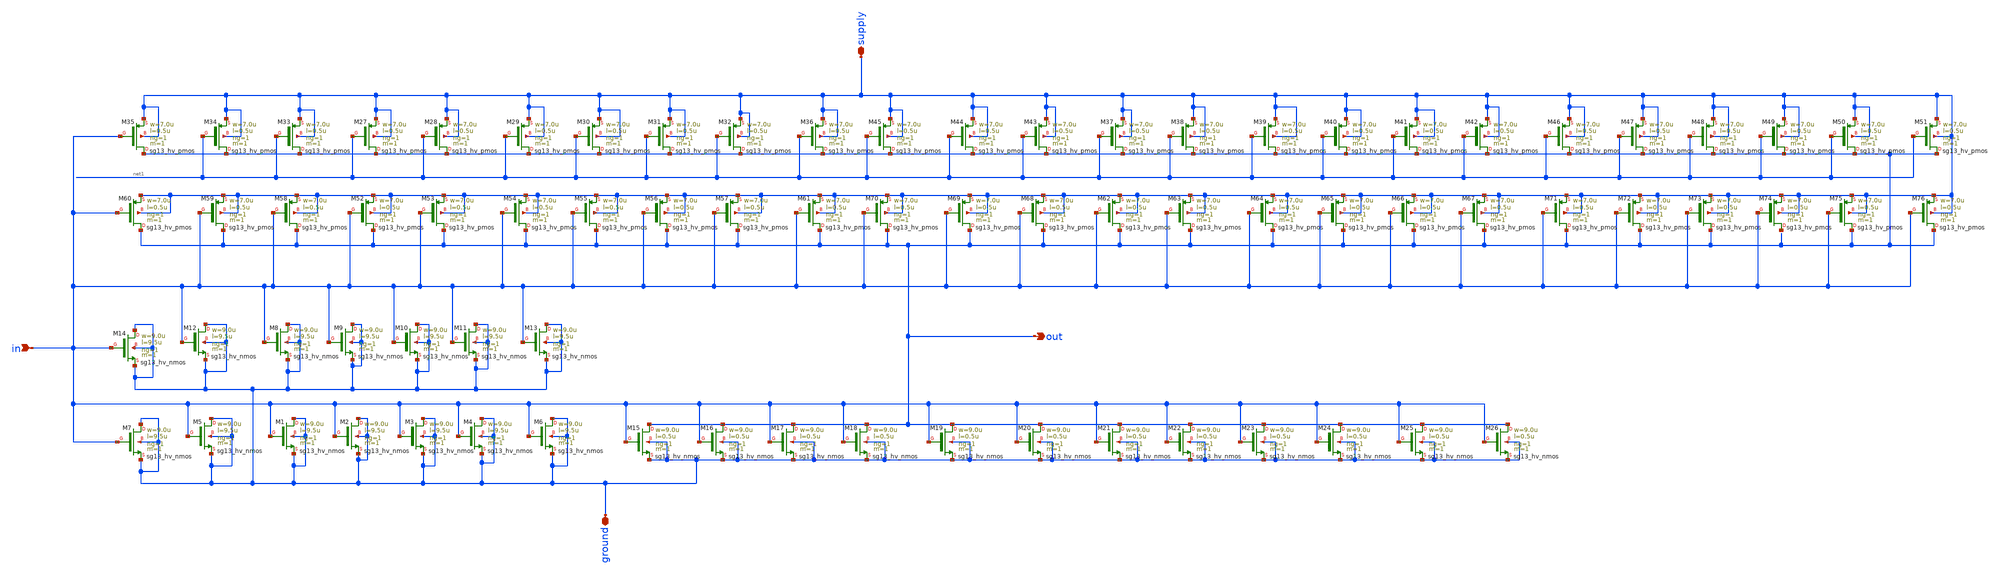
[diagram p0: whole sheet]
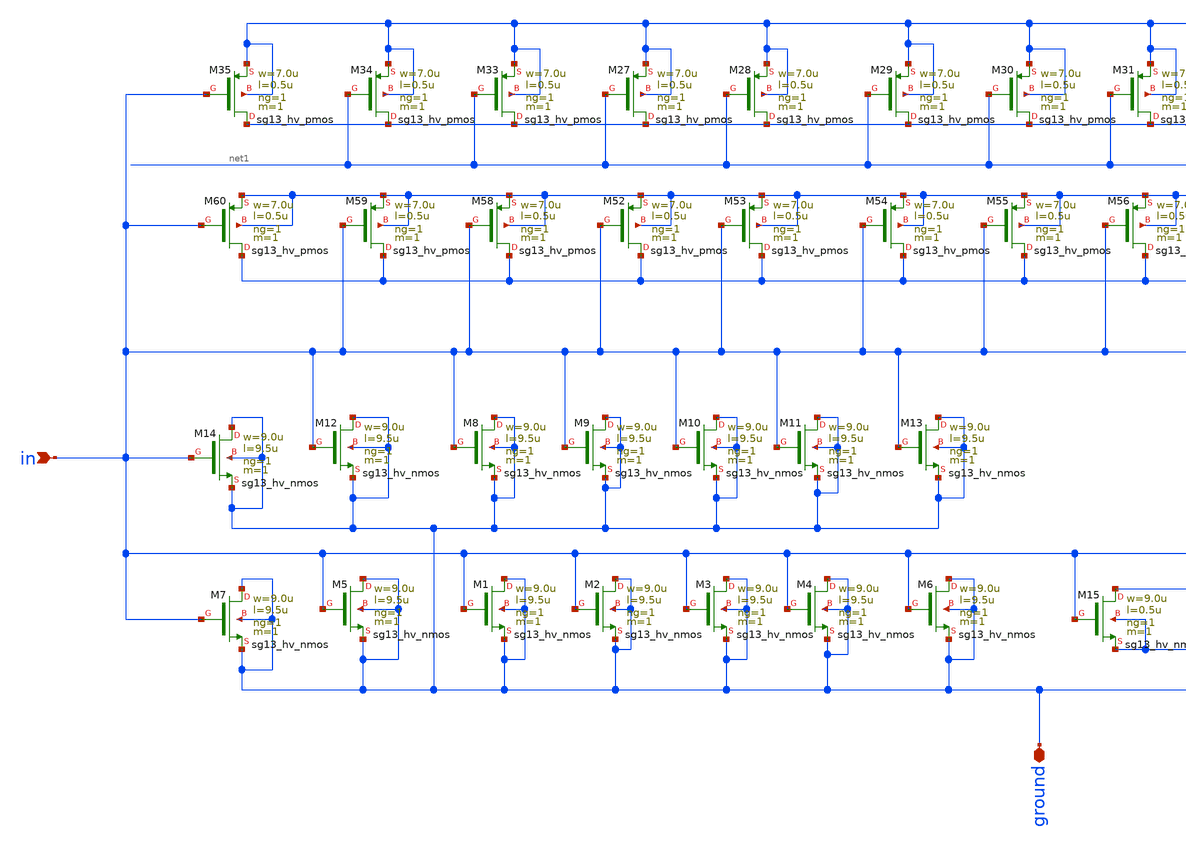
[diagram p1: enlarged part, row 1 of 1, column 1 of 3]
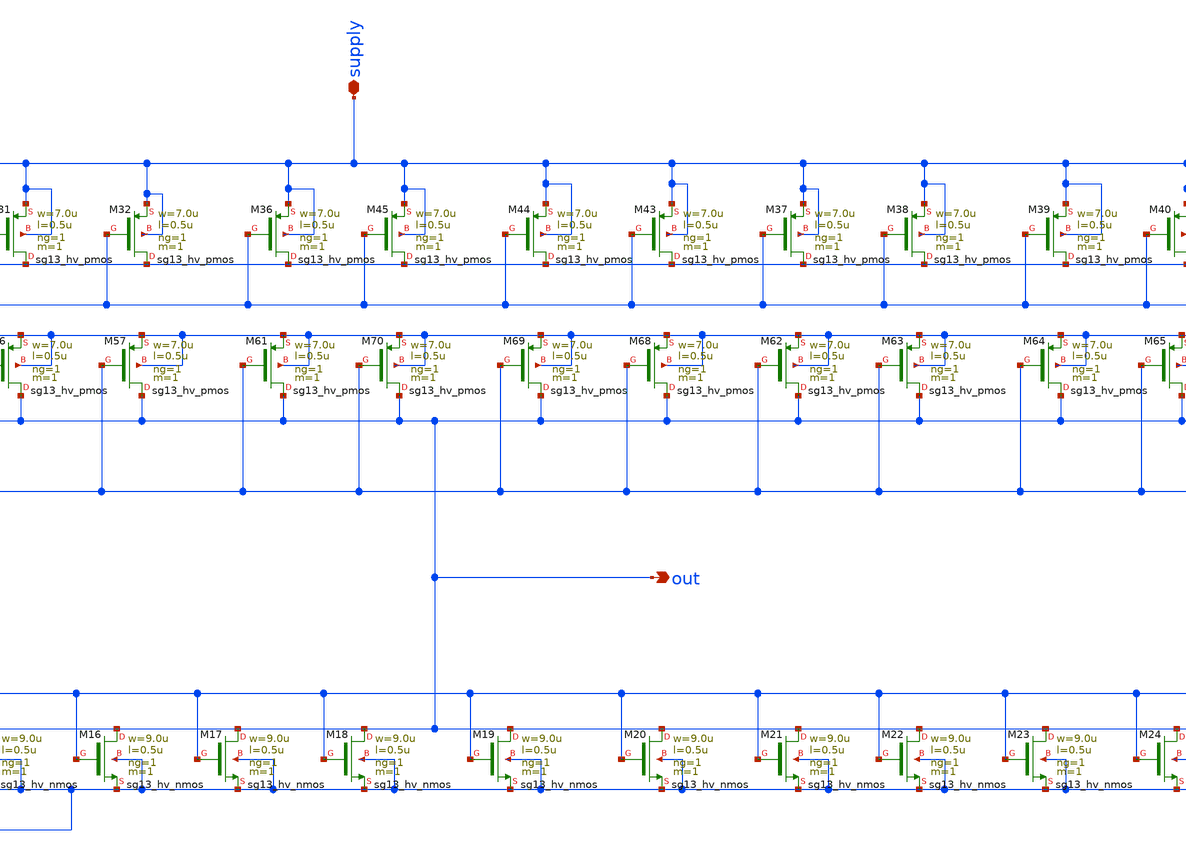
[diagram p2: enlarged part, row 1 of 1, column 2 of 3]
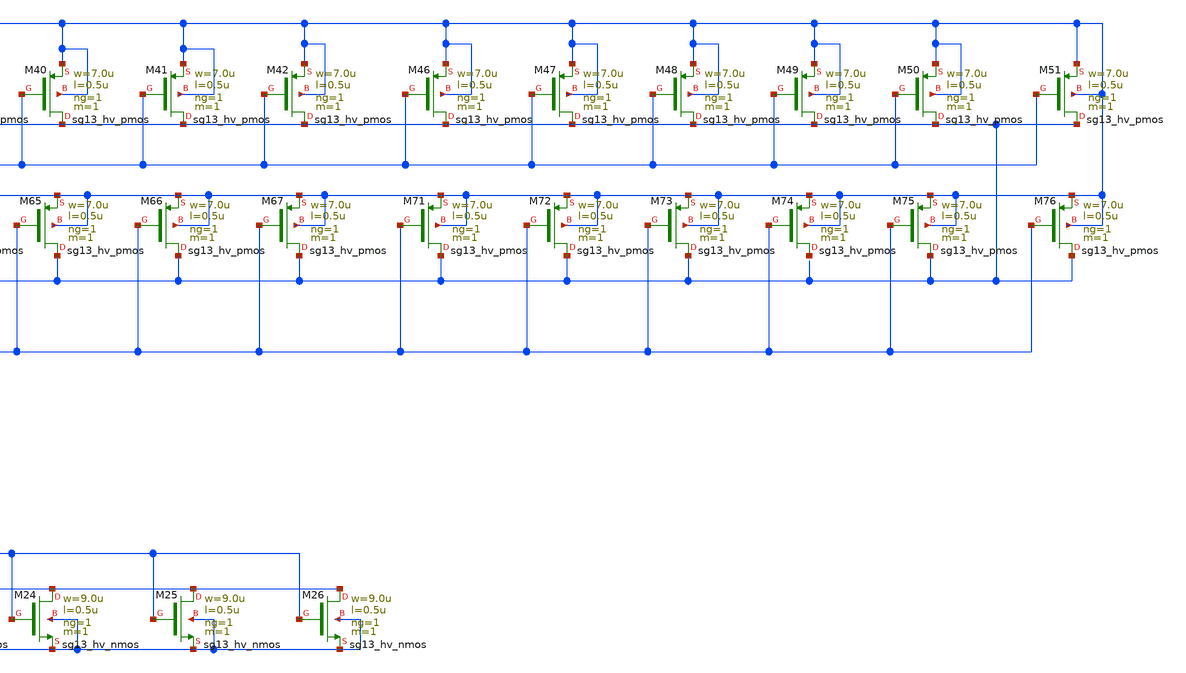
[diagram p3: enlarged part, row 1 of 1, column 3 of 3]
** sch_path: ihp-sg13g2/libs.ref/sg13g2_io/xschem/sg13g2_RCClampInverter.sch
**.subckt sg13g2_RCClampInverter supply ground out in
*.iopin supply
*.iopin ground
*.opin out
*.ipin in
XM1 ground in ground ground sg13_hv_nmos w=9.0u l=9.5u ng=1 m=1 mm_ok=1
XM2 ground in ground ground sg13_hv_nmos w=9.0u l=9.5u ng=1 m=1 mm_ok=1
XM3 ground in ground ground sg13_hv_nmos w=9.0u l=9.5u ng=1 m=1 mm_ok=1
XM4 ground in ground ground sg13_hv_nmos w=9.0u l=9.5u ng=1 m=1 mm_ok=1
XM5 ground in ground ground sg13_hv_nmos w=9.0u l=9.5u ng=1 m=1 mm_ok=1
XM6 ground in ground ground sg13_hv_nmos w=9.0u l=9.5u ng=1 m=1 mm_ok=1
XM7 ground in ground ground sg13_hv_nmos w=9.0u l=9.5u ng=1 m=1 mm_ok=1
XM8 ground in ground ground sg13_hv_nmos w=9.0u l=9.5u ng=1 m=1 mm_ok=1
XM9 ground in ground ground sg13_hv_nmos w=9.0u l=9.5u ng=1 m=1 mm_ok=1
XM10 ground in ground ground sg13_hv_nmos w=9.0u l=9.5u ng=1 m=1 mm_ok=1
XM11 ground in ground ground sg13_hv_nmos w=9.0u l=9.5u ng=1 m=1 mm_ok=1
XM12 ground in ground ground sg13_hv_nmos w=9.0u l=9.5u ng=1 m=1 mm_ok=1
XM13 ground in ground ground sg13_hv_nmos w=9.0u l=9.5u ng=1 m=1 mm_ok=1
XM14 ground in ground ground sg13_hv_nmos w=9.0u l=9.5u ng=1 m=1 mm_ok=1
XM15 out in ground ground sg13_hv_nmos w=9.0u l=0.5u ng=1 m=1 mm_ok=1
XM16 out in ground ground sg13_hv_nmos w=9.0u l=0.5u ng=1 m=1 mm_ok=1
XM17 out in ground ground sg13_hv_nmos w=9.0u l=0.5u ng=1 m=1 mm_ok=1
XM18 out in ground ground sg13_hv_nmos w=9.0u l=0.5u ng=1 m=1 mm_ok=1
XM19 out in ground ground sg13_hv_nmos w=9.0u l=0.5u ng=1 m=1 mm_ok=1
XM20 out in ground ground sg13_hv_nmos w=9.0u l=0.5u ng=1 m=1 mm_ok=1
XM21 out in ground ground sg13_hv_nmos w=9.0u l=0.5u ng=1 m=1 mm_ok=1
XM22 out in ground ground sg13_hv_nmos w=9.0u l=0.5u ng=1 m=1 mm_ok=1
XM23 out in ground ground sg13_hv_nmos w=9.0u l=0.5u ng=1 m=1 mm_ok=1
XM24 out in ground ground sg13_hv_nmos w=9.0u l=0.5u ng=1 m=1 mm_ok=1
XM25 out in ground ground sg13_hv_nmos w=9.0u l=0.5u ng=1 m=1 mm_ok=1
XM26 out in ground ground sg13_hv_nmos w=9.0u l=0.5u ng=1 m=1 mm_ok=1
XM27 out net1 supply supply sg13_hv_pmos w=7.0u l=0.5u ng=1 m=1 mm_ok=1
XM28 out net1 supply supply sg13_hv_pmos w=7.0u l=0.5u ng=1 m=1 mm_ok=1
XM29 out net1 supply supply sg13_hv_pmos w=7.0u l=0.5u ng=1 m=1 mm_ok=1
XM30 out net1 supply supply sg13_hv_pmos w=7.0u l=0.5u ng=1 m=1 mm_ok=1
XM31 out net1 supply supply sg13_hv_pmos w=7.0u l=0.5u ng=1 m=1 mm_ok=1
XM32 out net1 supply supply sg13_hv_pmos w=7.0u l=0.5u ng=1 m=1 mm_ok=1
XM33 out net1 supply supply sg13_hv_pmos w=7.0u l=0.5u ng=1 m=1 mm_ok=1
XM34 out net1 supply supply sg13_hv_pmos w=7.0u l=0.5u ng=1 m=1 mm_ok=1
XM35 out in supply supply sg13_hv_pmos w=7.0u l=0.5u ng=1 m=1 mm_ok=1
XM36 out net1 supply supply sg13_hv_pmos w=7.0u l=0.5u ng=1 m=1 mm_ok=1
XM37 out net1 supply supply sg13_hv_pmos w=7.0u l=0.5u ng=1 m=1 mm_ok=1
XM38 out net1 supply supply sg13_hv_pmos w=7.0u l=0.5u ng=1 m=1 mm_ok=1
XM39 out net1 supply supply sg13_hv_pmos w=7.0u l=0.5u ng=1 m=1 mm_ok=1
XM40 out net1 supply supply sg13_hv_pmos w=7.0u l=0.5u ng=1 m=1 mm_ok=1
XM41 out net1 supply supply sg13_hv_pmos w=7.0u l=0.5u ng=1 m=1 mm_ok=1
XM42 out net1 supply supply sg13_hv_pmos w=7.0u l=0.5u ng=1 m=1 mm_ok=1
XM43 out net1 supply supply sg13_hv_pmos w=7.0u l=0.5u ng=1 m=1 mm_ok=1
XM44 out net1 supply supply sg13_hv_pmos w=7.0u l=0.5u ng=1 m=1 mm_ok=1
XM45 out net1 supply supply sg13_hv_pmos w=7.0u l=0.5u ng=1 m=1 mm_ok=1
XM46 out net1 supply supply sg13_hv_pmos w=7.0u l=0.5u ng=1 m=1 mm_ok=1
XM47 out net1 supply supply sg13_hv_pmos w=7.0u l=0.5u ng=1 m=1 mm_ok=1
XM48 out net1 supply supply sg13_hv_pmos w=7.0u l=0.5u ng=1 m=1 mm_ok=1
XM49 out net1 supply supply sg13_hv_pmos w=7.0u l=0.5u ng=1 m=1 mm_ok=1
XM50 out net1 supply supply sg13_hv_pmos w=7.0u l=0.5u ng=1 m=1 mm_ok=1
XM51 out net1 supply supply sg13_hv_pmos w=7.0u l=0.5u ng=1 m=1 mm_ok=1
XM52 out in supply supply sg13_hv_pmos w=7.0u l=0.5u ng=1 m=1 mm_ok=1
XM53 out in supply supply sg13_hv_pmos w=7.0u l=0.5u ng=1 m=1 mm_ok=1
XM54 out in supply supply sg13_hv_pmos w=7.0u l=0.5u ng=1 m=1 mm_ok=1
XM55 out in supply supply sg13_hv_pmos w=7.0u l=0.5u ng=1 m=1 mm_ok=1
XM56 out in supply supply sg13_hv_pmos w=7.0u l=0.5u ng=1 m=1 mm_ok=1
XM57 out in supply supply sg13_hv_pmos w=7.0u l=0.5u ng=1 m=1 mm_ok=1
XM58 out in supply supply sg13_hv_pmos w=7.0u l=0.5u ng=1 m=1 mm_ok=1
XM59 out in supply supply sg13_hv_pmos w=7.0u l=0.5u ng=1 m=1 mm_ok=1
XM60 out in supply supply sg13_hv_pmos w=7.0u l=0.5u ng=1 m=1 mm_ok=1
XM61 out in supply supply sg13_hv_pmos w=7.0u l=0.5u ng=1 m=1 mm_ok=1
XM62 out in supply supply sg13_hv_pmos w=7.0u l=0.5u ng=1 m=1 mm_ok=1
XM63 out in supply supply sg13_hv_pmos w=7.0u l=0.5u ng=1 m=1 mm_ok=1
XM64 out in supply supply sg13_hv_pmos w=7.0u l=0.5u ng=1 m=1 mm_ok=1
XM65 out in supply supply sg13_hv_pmos w=7.0u l=0.5u ng=1 m=1 mm_ok=1
XM66 out in supply supply sg13_hv_pmos w=7.0u l=0.5u ng=1 m=1 mm_ok=1
XM67 out in supply supply sg13_hv_pmos w=7.0u l=0.5u ng=1 m=1 mm_ok=1
XM68 out in supply supply sg13_hv_pmos w=7.0u l=0.5u ng=1 m=1 mm_ok=1
XM69 out in supply supply sg13_hv_pmos w=7.0u l=0.5u ng=1 m=1 mm_ok=1
XM70 out in supply supply sg13_hv_pmos w=7.0u l=0.5u ng=1 m=1 mm_ok=1
XM71 out in supply supply sg13_hv_pmos w=7.0u l=0.5u ng=1 m=1 mm_ok=1
XM72 out in supply supply sg13_hv_pmos w=7.0u l=0.5u ng=1 m=1 mm_ok=1
XM73 out in supply supply sg13_hv_pmos w=7.0u l=0.5u ng=1 m=1 mm_ok=1
XM74 net2 in supply supply sg13_hv_pmos w=7.0u l=0.5u ng=1 m=1 mm_ok=1
XM75 out in supply supply sg13_hv_pmos w=7.0u l=0.5u ng=1 m=1 mm_ok=1
XM76 out in supply supply sg13_hv_pmos w=7.0u l=0.5u ng=1 m=1 mm_ok=1
**.ends
.end
